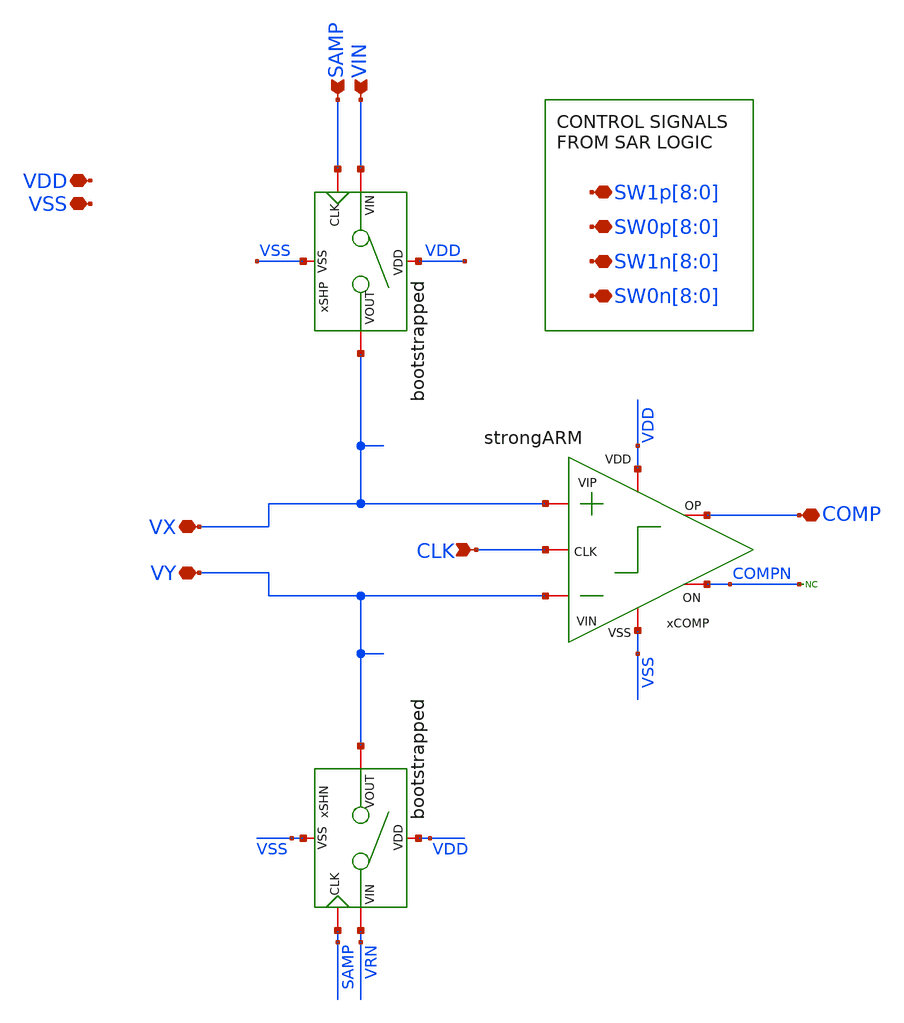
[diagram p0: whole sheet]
** sch_path: designs/sar_adc/top/VDAC/xschem/VDAC.sch
**.subckt VDAC VIN VY VX SAMP COMP
*+ SW1p[8],SW1p[7],SW1p[6],SW1p[5],SW1p[4],SW1p[3],SW1p[2],SW1p[1],SW1p[0] SW0p[8],SW0p[7],SW0p[6],SW0p[5],SW0p[4],SW0p[3],SW0p[2],SW0p[1],SW0p[0]
*+ SW1n[8],SW1n[7],SW1n[6],SW1n[5],SW1n[4],SW1n[3],SW1n[2],SW1n[1],SW1n[0] SW0n[8],SW0n[7],SW0n[6],SW0n[5],SW0n[4],SW0n[3],SW0n[2],SW0n[1],SW0n[0] CLK VSS VDD
*.ipin VIN
*.iopin VY
*.iopin VX
*.ipin SAMP
*.iopin COMP
*.iopin SW1p[8],SW1p[7],SW1p[6],SW1p[5],SW1p[4],SW1p[3],SW1p[2],SW1p[1],SW1p[0]
*.iopin SW0p[8],SW0p[7],SW0p[6],SW0p[5],SW0p[4],SW0p[3],SW0p[2],SW0p[1],SW0p[0]
*.iopin SW1n[8],SW1n[7],SW1n[6],SW1n[5],SW1n[4],SW1n[3],SW1n[2],SW1n[1],SW1n[0]
*.iopin SW0n[8],SW0n[7],SW0n[6],SW0n[5],SW0n[4],SW0n[3],SW0n[2],SW0n[1],SW0n[0]
*.ipin CLK
*.iopin VSS
*.iopin VDD
xSHP VDD VSS SAMP VIN VX bootstrapped
xSHN VDD VSS SAMP VRN VY bootstrapped
xCOMP VDD CLK COMPN COMP VY VX VSS strongARM
* noconn COMPN
**.ends
.end
